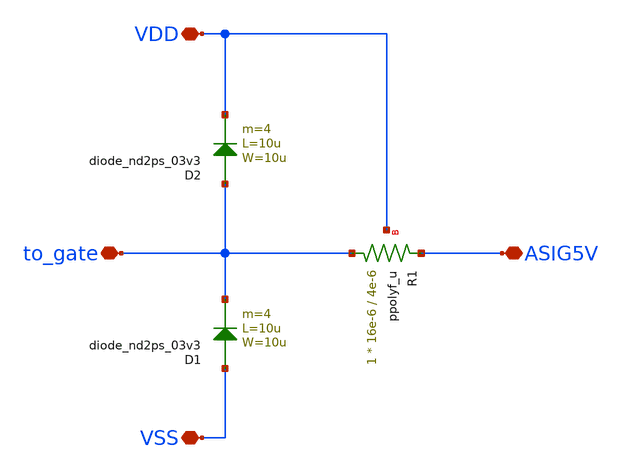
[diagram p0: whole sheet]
** sch_path: src/design_xsch/CMD_ESD_prot.sch
**.subckt CMD_ESD_prot VDD to_gate VSS ASIG5V
*.iopin VDD
*.iopin to_gate
*.iopin VSS
*.iopin ASIG5V
XR1 to_gate ASIG5V VDD ppolyf_u r_width=16e-6 r_length=4e-6 m=1
D1 VSS to_gate diode_nd2ps_03v3 area='10u * 10u ' pj='2*10u + 2*10u ' m=4
D2 to_gate VDD diode_nd2ps_03v3 area='10u * 10u ' pj='2*10u + 2*10u ' m=4
**.ends
.end
